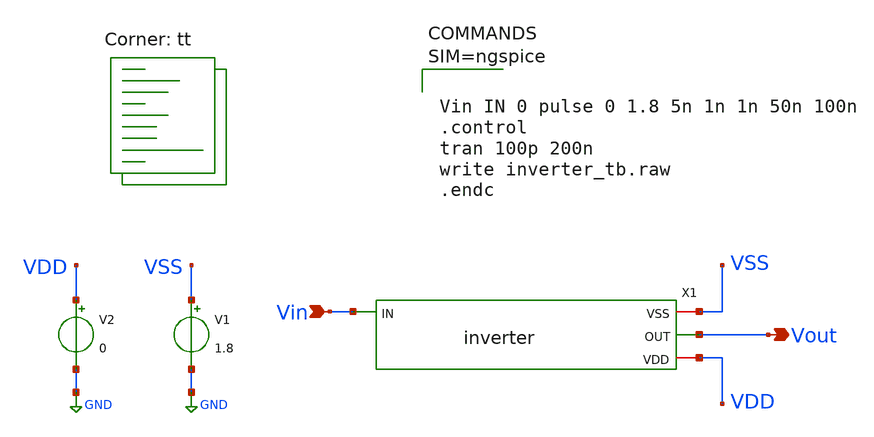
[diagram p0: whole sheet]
** sch_path: xschem/inverter_tb.sch
**.subckt inverter_tb Vin Vout
*.ipin Vin
*.opin Vout
V1 VSS GND 1.8
X1 VSS Vin Vout VDD inverter
V2 VDD GND 0
**** begin user architecture code

** opencircuitdesign pdks install
.lib $::SKYWATER_MODELS/sky130.lib.spice tt




Vin IN 0 pulse 0 1.8 5n 1n 1n 50n 100n
.control
tran 100p 200n
write inverter_tb.raw
.endc



.lib $::SKYWATER_MODELS/sky130.lib.spice tt
**** end user architecture code
**.ends

* expanding   symbol:  inverter.sym # of pins=4
** sym_path: xschem/inverter.sym
** sch_path: xschem/inverter.sch
.subckt inverter VSS IN OUT VDD
*.ipin IN
*.opin OUT
*.iopin VDD
*.iopin VSS
XM1 OUT IN VSS VSS sky130_fd_pr__nfet_01v8 L=0.15 W=1 nf=1 ad='int((nf+1)/2) * W/nf * 0.29' as='int((nf+2)/2) * W/nf * 0.29'
+ pd='2*int((nf+1)/2) * (W/nf + 0.29)' ps='2*int((nf+2)/2) * (W/nf + 0.29)' nrd='0.29 / W' nrs='0.29 / W'
+ sa=0 sb=0 sd=0 mult=1 m=1
XM2 OUT IN VDD VDD sky130_fd_pr__pfet_01v8 L=0.15 W=1 nf=1 ad='int((nf+1)/2) * W/nf * 0.29' as='int((nf+2)/2) * W/nf * 0.29'
+ pd='2*int((nf+1)/2) * (W/nf + 0.29)' ps='2*int((nf+2)/2) * (W/nf + 0.29)' nrd='0.29 / W' nrs='0.29 / W'
+ sa=0 sb=0 sd=0 mult=1 m=1
.ends

.GLOBAL GND
.end
